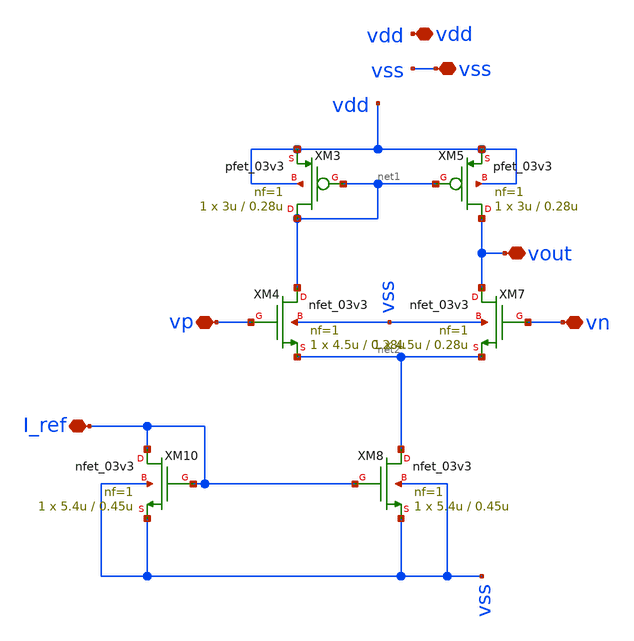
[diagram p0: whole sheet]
** sch_path: designs/libs/core_LIF_comp/core_ota_1stage/ota_1stage.sch
**.subckt ota_1stage vdd vss vp vn vout I_ref
*.iopin vdd
*.iopin vss
*.iopin vp
*.iopin vn
*.iopin vout
*.iopin I_ref
XM3 net1 net1 vdd vdd pfet_03v3 L=0.28u W=3u nf=1 ad='int((nf+1)/2) * W/nf * 0.18u' as='int((nf+2)/2) * W/nf * 0.18u'
+ pd='2*int((nf+1)/2) * (W/nf + 0.18u)' ps='2*int((nf+2)/2) * (W/nf + 0.18u)' nrd='0.18u / W' nrs='0.18u / W'
+ sa=0 sb=0 sd=0 m=1
XM4 net1 vp net2 vss nfet_03v3 L=0.28u W=4.5u nf=1 ad='int((nf+1)/2) * W/nf * 0.18u' as='int((nf+2)/2) * W/nf * 0.18u'
+ pd='2*int((nf+1)/2) * (W/nf + 0.18u)' ps='2*int((nf+2)/2) * (W/nf + 0.18u)' nrd='0.18u / W' nrs='0.18u / W'
+ sa=0 sb=0 sd=0 m=1
XM5 vout net1 vdd vdd pfet_03v3 L=0.28u W=3u nf=1 ad='int((nf+1)/2) * W/nf * 0.18u' as='int((nf+2)/2) * W/nf * 0.18u'
+ pd='2*int((nf+1)/2) * (W/nf + 0.18u)' ps='2*int((nf+2)/2) * (W/nf + 0.18u)' nrd='0.18u / W' nrs='0.18u / W'
+ sa=0 sb=0 sd=0 m=1
XM7 vout vn net2 vss nfet_03v3 L=0.28u W=4.5u nf=1 ad='int((nf+1)/2) * W/nf * 0.18u' as='int((nf+2)/2) * W/nf * 0.18u'
+ pd='2*int((nf+1)/2) * (W/nf + 0.18u)' ps='2*int((nf+2)/2) * (W/nf + 0.18u)' nrd='0.18u / W' nrs='0.18u / W'
+ sa=0 sb=0 sd=0 m=1
XM8 net2 I_ref vss vss nfet_03v3 L=0.45u W=5.4u nf=1 ad='int((nf+1)/2) * W/nf * 0.18u' as='int((nf+2)/2) * W/nf * 0.18u'
+ pd='2*int((nf+1)/2) * (W/nf + 0.18u)' ps='2*int((nf+2)/2) * (W/nf + 0.18u)' nrd='0.18u / W' nrs='0.18u / W'
+ sa=0 sb=0 sd=0 m=1
XM10 I_ref I_ref vss vss nfet_03v3 L=0.45u W=5.4u nf=1 ad='int((nf+1)/2) * W/nf * 0.18u' as='int((nf+2)/2) * W/nf * 0.18u'
+ pd='2*int((nf+1)/2) * (W/nf + 0.18u)' ps='2*int((nf+2)/2) * (W/nf + 0.18u)' nrd='0.18u / W' nrs='0.18u / W'
+ sa=0 sb=0 sd=0 m=1
**.ends
.end
